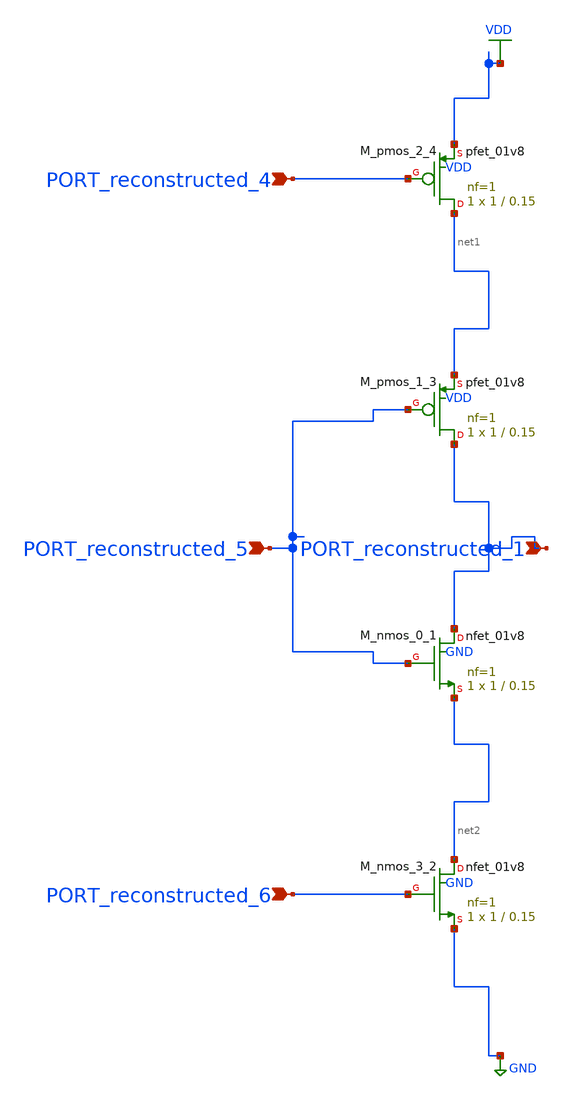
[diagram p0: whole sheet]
** sch_path: schematics/SchemGen/raster_p08_002_crop1.sch
**.subckt raster_p08_002_crop1 PORT_reconstructed_5 PORT_reconstructed_4 PORT_reconstructed_1
*+ PORT_reconstructed_6
*.ipin PORT_reconstructed_5
*.ipin PORT_reconstructed_4
*.ipin PORT_reconstructed_1
*.ipin PORT_reconstructed_6
XM_nmos_0_1 PORT_reconstructed_1 PORT_reconstructed_5 net2 GND sky130_fd_pr__nfet_01v8 L=0.15 W=1 nf=1
+ ad='int((1 + 1)/2) * 1 / 1 * 0.29' as='int((1 + 2)/2) * 1 / 1 * 0.29' pd='2*int((1 + 1)/2) * (1 / 1 + 0.29)'
+ ps='2*int((1 + 2)/2) * (1 / 1 + 0.29)' nrd='0.29 / 1 ' nrs='0.29 / 1 ' sa=0 sb=0 sd=0 mult=1 m=1
XM_nmos_3_2 net2 PORT_reconstructed_6 GND GND sky130_fd_pr__nfet_01v8 L=0.15 W=1 nf=1 ad='int((1 + 1)/2) * 1 / 1 * 0.29'
+ as='int((1 + 2)/2) * 1 / 1 * 0.29' pd='2*int((1 + 1)/2) * (1 / 1 + 0.29)' ps='2*int((1 + 2)/2) * (1 / 1 + 0.29)'
+ nrd='0.29 / 1 ' nrs='0.29 / 1 ' sa=0 sb=0 sd=0 mult=1 m=1
XM_pmos_1_3 PORT_reconstructed_1 PORT_reconstructed_5 net1 VDD sky130_fd_pr__pfet_01v8 L=0.15 W=1 nf=1
+ ad='int((1 + 1)/2) * 1 / 1 * 0.29' as='int((1 + 2)/2) * 1 / 1 * 0.29' pd='2*int((1 + 1)/2) * (1 / 1 + 0.29)'
+ ps='2*int((1 + 2)/2) * (1 / 1 + 0.29)' nrd='0.29 / 1 ' nrs='0.29 / 1 ' sa=0 sb=0 sd=0 mult=1 m=1
XM_pmos_2_4 net1 PORT_reconstructed_4 VDD VDD sky130_fd_pr__pfet_01v8 L=0.15 W=1 nf=1 ad='int((1 + 1)/2) * 1 / 1 * 0.29'
+ as='int((1 + 2)/2) * 1 / 1 * 0.29' pd='2*int((1 + 1)/2) * (1 / 1 + 0.29)' ps='2*int((1 + 2)/2) * (1 / 1 + 0.29)'
+ nrd='0.29 / 1 ' nrs='0.29 / 1 ' sa=0 sb=0 sd=0 mult=1 m=1
**.ends
.GLOBAL GND
.GLOBAL VDD
.end
